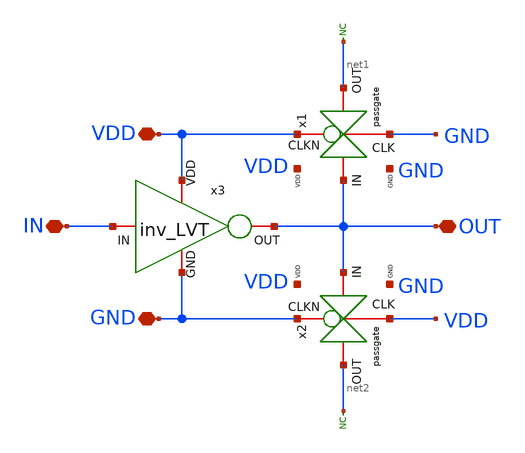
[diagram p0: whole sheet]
** sch_path: LVT/rovcel2_LVT/rovcel2_LVT.sch
**.subckt rovcel2_LVT OUT IN VDD GND
*.iopin OUT
*.iopin IN
*.iopin VDD
*.iopin GND
* noconn #net1
* noconn #net2
x2 GND OUT net2 VDD GND VDD passgate
x3 VDD IN OUT GND inv_LVT
x1 VDD OUT net1 GND GND VDD passgate
**.ends
.GLOBAL VDD
.GLOBAL GND
.end
